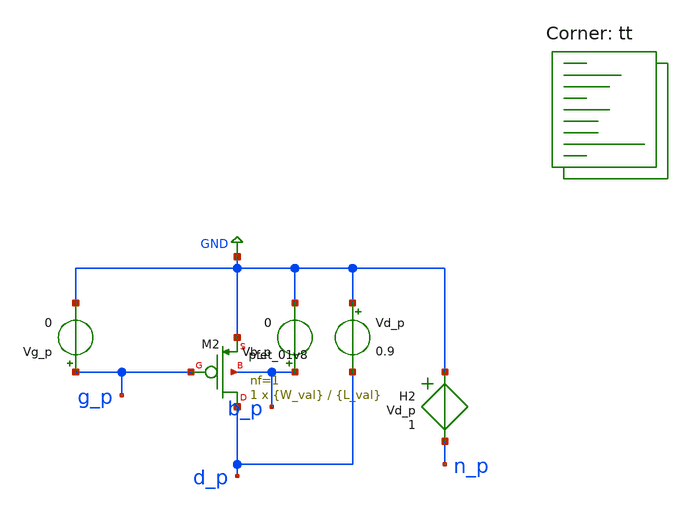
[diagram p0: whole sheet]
** sch_path: xschem/Testing2.sch
**.subckt Testing2
XM2 d_p g_p GND b_p sky130_fd_pr__pfet_01v8 L={L_val} W={W_val} nf=1 ad='int((1 + 1)/2) * {W_val} / 1 * 0.29'
+ as='int((1 + 2)/2) * {W_val} / 1 * 0.29' pd='2*int((1 + 1)/2) * ({W_val} / 1 + 0.29)' ps='2*int((1 + 2)/2) * ({W_val} / 1 + 0.29)'
+ nrd='0.29 / {W_val} ' nrs='0.29 / {W_val} ' sa=0 sb=0 sd=0 mult=1 m=1
H2 GND n_p Vd_p 1
Vg_p g_p GND 0
Vd_p GND d_p 0.9
Vb_p b_p GND 0
**** begin user architecture code


* gm/ID Characterization for Sky130 nfet_01v8
* Parameters
.param W_val = 10
.param L_val = 1.0
.dc Vg_p 0 -1.8 -0.01

.save all @m.xm2.msky130_fd_pr__pfet_01v8[id]
.save @m.xm2.msky130_fd_pr__pfet_01v8[vth]
.save @m.xm2.msky130_fd_pr__pfet_01v8[gm]
.save @m.xm2.msky130_fd_pr__pfet_01v8[cgg]
.save @m.xm2.msky130_fd_pr__pfet_01v8[w]
.save @m.xm2.msky130_fd_pr__pfet_01v8[l]
.save @m.xm2.msky130_fd_pr__pfet_01v8[gds]


.control

  * Direct Plotting in ngspice
  set xbrushwidth=2

 foreach val 1.5 3.0 3.0
  run
  let W_n = @m.xm2.msky130_fd_pr__pfet_01v8[w]
  let L_n = @m.xm2.msky130_fd_pr__pfet_01v8[l]
  let g_m_n = @m.xm2.msky130_fd_pr__pfet_01v8[gm]
  let i_d_n = @m.xm2.msky130_fd_pr__pfet_01v8[id]
  let v_th_n = @m.xm2.msky130_fd_pr__pfet_01v8[vth]
  let c_gg_n =  @m.xm2.msky130_fd_pr__pfet_01v8[cgg]
  let g_ds_n =  @m.xm2.msky130_fd_pr__pfet_01v8[gds]


  let gm_id_n = 'g_m_n/i_d_n'
  let v_ov_n = 'abs(v(g_p)) - abs(v_th_n)'

  let w_T_n = 'g_m_n/c_gg_n'
  let f_T_n = 'w_T_n/('2*pi')'

  let gm_gmds_n = 'g_m_n/g_ds_n'

  let id_W_n = 'i_d_n/W_n'

  alterparam L_val = $val
  reset
 end
  print dc1.L_n dc2.L_n dc3.L_n

  *plot $plot_id_W vs $plot_gm_id ylog xlabel 'Current Eff S/A' ylabel 'A/W' title 'NMOS Id/W vs gm/Id'
  *plot $plot_gm_gmds vs $plot_gm_id xlabel 'Current Eff S/A' ylabel 'Intrinsic Gain' title 'NMOS gm/Id vs gm/gds'
  *plot $plot_fT vs $plot_gm_id xlabel 'Current Eff S/A' ylabel 'Transit Frequency GHz' title 'NMOS Id/W vs fT'
  *plot $plot_gm_id vs $plot_vov xlabel 'Overdrive Voltage V' ylabel 'Current Eff S/A' title 'NMOS gm/Id vs Vov'

  plot dc1.id_W_n vs dc1.gm_id_n dc2.id_W_n vs dc2.gm_id_n dc3.id_W_n vs dc3.gm_id_n xlabel 'Current Eff S/A'
+ ylabel 'A/W' title 'PMOS Id/W vs gm/Id'
  plot dc1.gm_gmds_n vs dc1.gm_id_n dc2.gm_gmds_n vs dc2.gm_id_n dc3.gm_gmds_n vs dc3.gm_id_n xlabel
+ 'Current Eff S/A' ylabel 'Intrinsic Gain' title 'PMOS gm/Id vs gm/gds'
  plot dc1.f_T_n vs dc1.gm_id_n dc2.f_T_n vs dc2.gm_id_n dc3.f_T_n vs dc3.gm_id_n xlabel 'Current Eff S/A'
+ ylabel 'Transit Frequency GHz' title 'PMOS Id/W vs fT'
  plot dc1.gm_id_n vs dc1.v_ov_n dc2.gm_id_n vs dc2.v_ov_n dc3.gm_id_n vs dc3.v_ov_n xlabel 'Overdrive Voltage V'
+ ylabel 'Current Eff S/A' title 'NMOS gm/Id vs Vov'
  plot dc1.gm_id_n dc2.gm_id_n dc3.gm_id_n xlabel 'Overdrive Voltage V' ylabel 'Current Eff S/A' title
+ 'NMOS gm/Id vs Vsg'


.endc
.end

.lib $::SKYWATER_MODELS/sky130.lib.spice tt
**** end user architecture code
**.ends
.GLOBAL GND
.end
